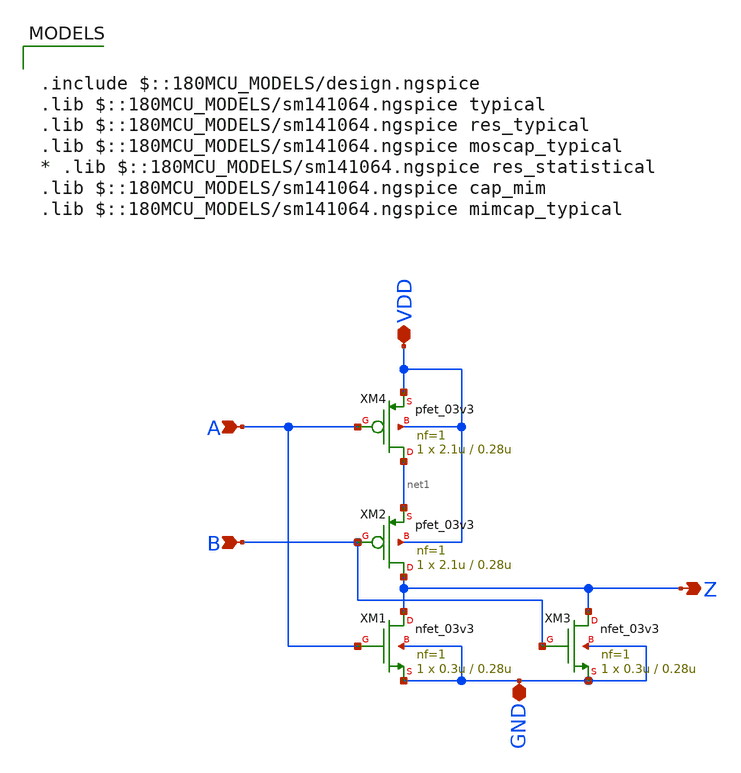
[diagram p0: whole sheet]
** sch_path: pll_block_templates_v1/layout2/nor.sch
**.subckt nor A B Z GND VDD
*.ipin A
*.ipin B
*.opin Z
*.iopin GND
*.iopin VDD
XM1 Z A GND GND nfet_03v3 L=0.28u W=0.3u nf=1 ad='int((nf+1)/2) * W/nf * 0.18u' as='int((nf+2)/2) * W/nf * 0.18u'
+ pd='2*int((nf+1)/2) * (W/nf + 0.18u)' ps='2*int((nf+2)/2) * (W/nf + 0.18u)' nrd='0.18u / W' nrs='0.18u / W'
+ sa=0 sb=0 sd=0 m=1
XM2 Z B net1 VDD pfet_03v3 L=0.28u W=2.1u nf=1 ad='int((nf+1)/2) * W/nf * 0.18u' as='int((nf+2)/2) * W/nf * 0.18u'
+ pd='2*int((nf+1)/2) * (W/nf + 0.18u)' ps='2*int((nf+2)/2) * (W/nf + 0.18u)' nrd='0.18u / W' nrs='0.18u / W'
+ sa=0 sb=0 sd=0 m=1
XM3 Z B GND GND nfet_03v3 L=0.28u W=0.3u nf=1 ad='int((nf+1)/2) * W/nf * 0.18u' as='int((nf+2)/2) * W/nf * 0.18u'
+ pd='2*int((nf+1)/2) * (W/nf + 0.18u)' ps='2*int((nf+2)/2) * (W/nf + 0.18u)' nrd='0.18u / W' nrs='0.18u / W'
+ sa=0 sb=0 sd=0 m=1
XM4 net1 A VDD VDD pfet_03v3 L=0.28u W=2.1u nf=1 ad='int((nf+1)/2) * W/nf * 0.18u' as='int((nf+2)/2) * W/nf * 0.18u'
+ pd='2*int((nf+1)/2) * (W/nf + 0.18u)' ps='2*int((nf+2)/2) * (W/nf + 0.18u)' nrd='0.18u / W' nrs='0.18u / W'
+ sa=0 sb=0 sd=0 m=1
**** begin user architecture code

.include $::180MCU_MODELS/design.ngspice
.lib $::180MCU_MODELS/sm141064.ngspice typical
.lib $::180MCU_MODELS/sm141064.ngspice res_typical
.lib $::180MCU_MODELS/sm141064.ngspice moscap_typical
* .lib $::180MCU_MODELS/sm141064.ngspice res_statistical
.lib $::180MCU_MODELS/sm141064.ngspice cap_mim
.lib $::180MCU_MODELS/sm141064.ngspice mimcap_typical

**** end user architecture code
**.ends
.end
